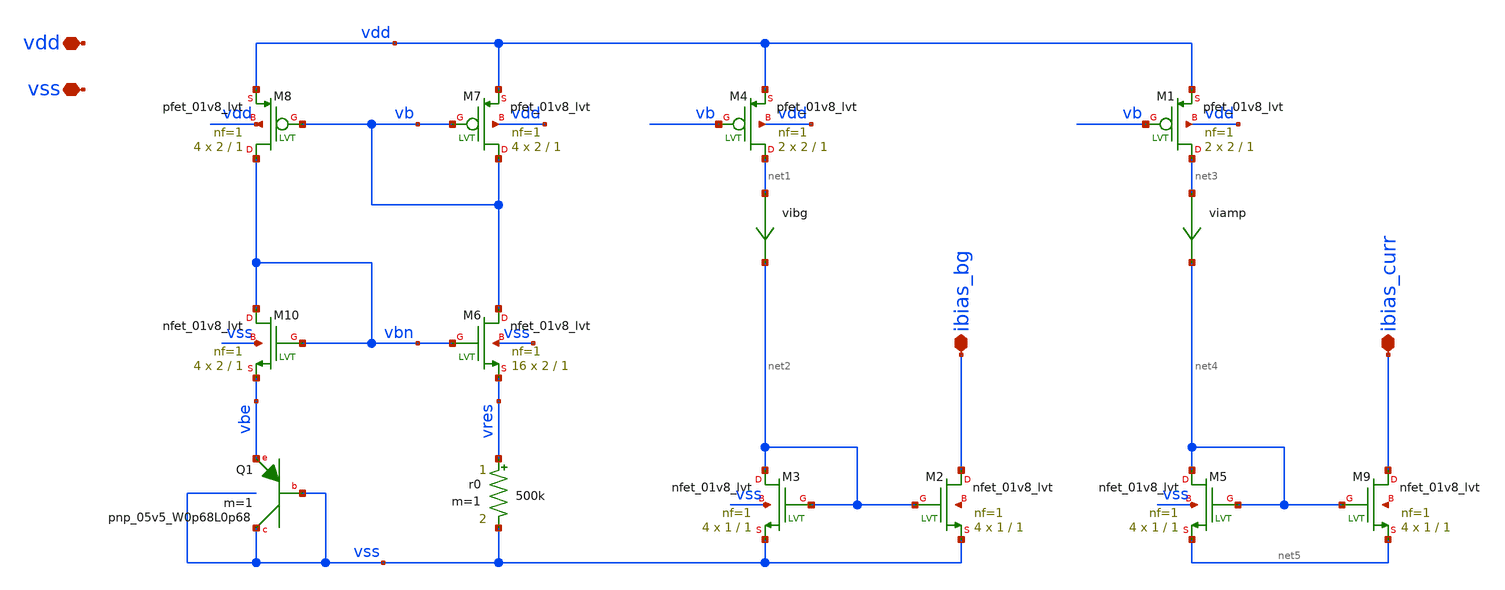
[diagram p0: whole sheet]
** sch_path: xschem/bias/bias_base_n.sch
**.subckt bias_base_n ibias_bg ibias_curr vdd vss
*.iopin ibias_bg
*.iopin ibias_curr
*.iopin vdd
*.iopin vss
r0 vres vss 500k m=1
XQ1 vss vss vbe sky130_fd_pr__pnp_05v5_W0p68L0p68 m=1
XM10 vbn vbn vbe vss sky130_fd_pr__nfet_01v8_lvt L=1 W=2 nf=1 ad='int((nf+1)/2) * W/nf * 0.29' as='int((nf+2)/2) * W/nf * 0.29'
+ pd='2*int((nf+1)/2) * (W/nf + 0.29)' ps='2*int((nf+2)/2) * (W/nf + 0.29)' nrd='0.29 / W' nrs='0.29 / W'
+ sa=0 sb=0 sd=0 mult=4 m=4
XM6 vb vbn vres vss sky130_fd_pr__nfet_01v8_lvt L=1 W=2 nf=1 ad='int((nf+1)/2) * W/nf * 0.29' as='int((nf+2)/2) * W/nf * 0.29'
+ pd='2*int((nf+1)/2) * (W/nf + 0.29)' ps='2*int((nf+2)/2) * (W/nf + 0.29)' nrd='0.29 / W' nrs='0.29 / W'
+ sa=0 sb=0 sd=0 mult=16 m=16
XM7 vb vb vdd vdd sky130_fd_pr__pfet_01v8_lvt L=1 W=2 nf=1 ad='int((nf+1)/2) * W/nf * 0.29' as='int((nf+2)/2) * W/nf * 0.29'
+ pd='2*int((nf+1)/2) * (W/nf + 0.29)' ps='2*int((nf+2)/2) * (W/nf + 0.29)' nrd='0.29 / W' nrs='0.29 / W'
+ sa=0 sb=0 sd=0 mult=4 m=4
XM8 vbn vb vdd vdd sky130_fd_pr__pfet_01v8_lvt L=1 W=2 nf=1 ad='int((nf+1)/2) * W/nf * 0.29' as='int((nf+2)/2) * W/nf * 0.29'
+ pd='2*int((nf+1)/2) * (W/nf + 0.29)' ps='2*int((nf+2)/2) * (W/nf + 0.29)' nrd='0.29 / W' nrs='0.29 / W'
+ sa=0 sb=0 sd=0 mult=4 m=4
XM4 net1 vb vdd vdd sky130_fd_pr__pfet_01v8_lvt L=1 W=2 nf=1 ad='int((nf+1)/2) * W/nf * 0.29' as='int((nf+2)/2) * W/nf * 0.29'
+ pd='2*int((nf+1)/2) * (W/nf + 0.29)' ps='2*int((nf+2)/2) * (W/nf + 0.29)' nrd='0.29 / W' nrs='0.29 / W'
+ sa=0 sb=0 sd=0 mult=2 m=2
vibg net1 net2 0
.save i(vibg)
viamp net3 net4 0
.save i(viamp)
XM3 net2 net2 vss vss sky130_fd_pr__nfet_01v8_lvt L=1 W=1 nf=1 ad='int((nf+1)/2) * W/nf * 0.29' as='int((nf+2)/2) * W/nf * 0.29'
+ pd='2*int((nf+1)/2) * (W/nf + 0.29)' ps='2*int((nf+2)/2) * (W/nf + 0.29)' nrd='0.29 / W' nrs='0.29 / W'
+ sa=0 sb=0 sd=0 mult=4 m=4
XM2 ibias_bg net2 vss net6 sky130_fd_pr__nfet_01v8_lvt L=1 W=1 nf=1 ad='int((nf+1)/2) * W/nf * 0.29'
+ as='int((nf+2)/2) * W/nf * 0.29' pd='2*int((nf+1)/2) * (W/nf + 0.29)' ps='2*int((nf+2)/2) * (W/nf + 0.29)'
+ nrd='0.29 / W' nrs='0.29 / W' sa=0 sb=0 sd=0 mult=4 m=4
XM1 net3 vb vdd vdd sky130_fd_pr__pfet_01v8_lvt L=1 W=2 nf=1 ad='int((nf+1)/2) * W/nf * 0.29' as='int((nf+2)/2) * W/nf * 0.29'
+ pd='2*int((nf+1)/2) * (W/nf + 0.29)' ps='2*int((nf+2)/2) * (W/nf + 0.29)' nrd='0.29 / W' nrs='0.29 / W'
+ sa=0 sb=0 sd=0 mult=2 m=2
XM5 net4 net4 net5 vss sky130_fd_pr__nfet_01v8_lvt L=1 W=1 nf=1 ad='int((nf+1)/2) * W/nf * 0.29' as='int((nf+2)/2) * W/nf * 0.29'
+ pd='2*int((nf+1)/2) * (W/nf + 0.29)' ps='2*int((nf+2)/2) * (W/nf + 0.29)' nrd='0.29 / W' nrs='0.29 / W'
+ sa=0 sb=0 sd=0 mult=4 m=4
XM9 ibias_curr net4 net5 net7 sky130_fd_pr__nfet_01v8_lvt L=1 W=1 nf=1 ad='int((nf+1)/2) * W/nf * 0.29'
+ as='int((nf+2)/2) * W/nf * 0.29' pd='2*int((nf+1)/2) * (W/nf + 0.29)' ps='2*int((nf+2)/2) * (W/nf + 0.29)'
+ nrd='0.29 / W' nrs='0.29 / W' sa=0 sb=0 sd=0 mult=4 m=4
**.ends
.end
